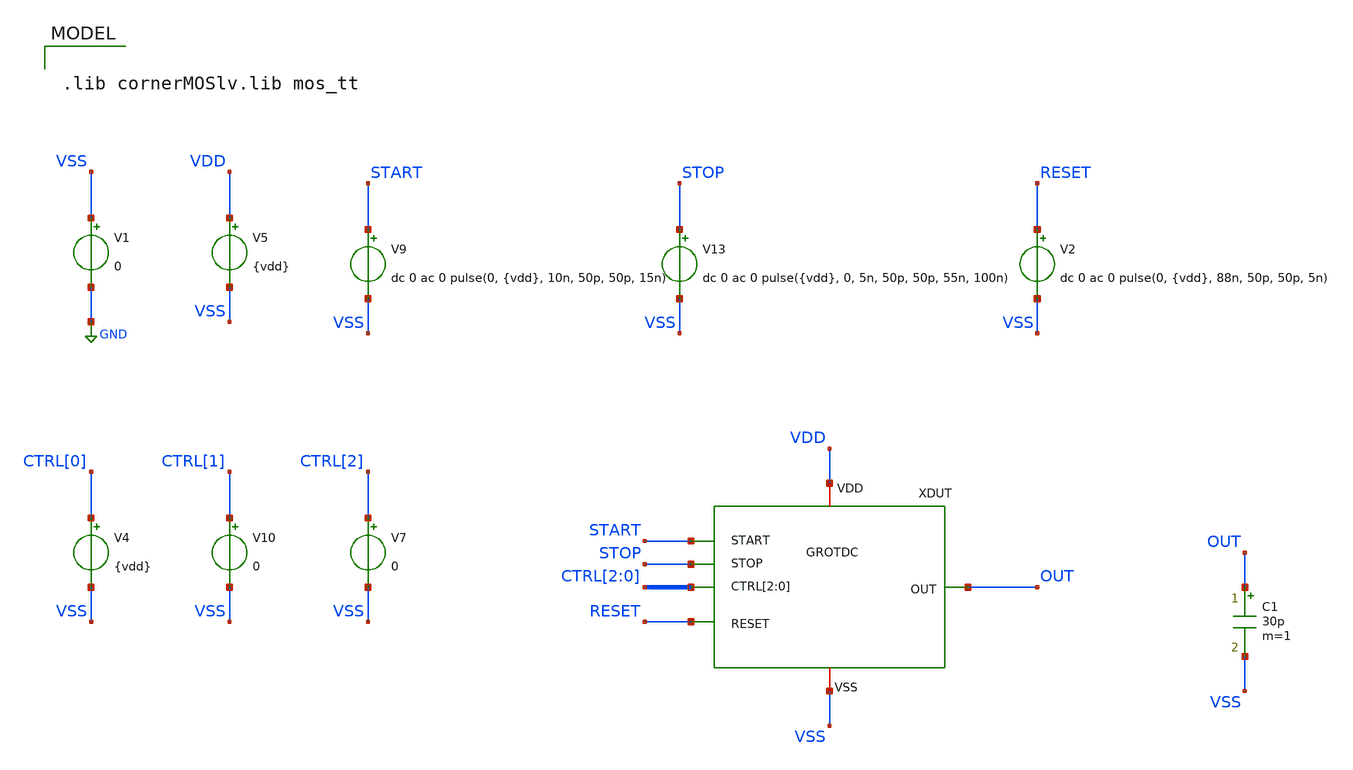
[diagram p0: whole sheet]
** sch_path: ADC8711-main/testbenches/tran/xschem/GROTDC_tb_final.sch
**.subckt GROTDC_tb_final
V1 VSS GND 0
V5 VDD VSS {vdd}
V9 START VSS dc 0 ac 0 pulse(0, {vdd}, 10n, 50p, 50p, 15n)
V13 STOP VSS dc 0 ac 0 pulse({vdd}, 0, 5n, 50p, 50p, 55n, 100n)
XDUT OUT VDD START STOP VSS RESET CTRL[2] CTRL[1] CTRL[0] GROTDC
V4 CTRL[0] VSS {vdd}
V10 CTRL[1] VSS 0
V7 CTRL[2] VSS 0
C1 OUT VSS 30p m=1
V2 RESET VSS dc 0 ac 0 pulse(0, {vdd}, 88n, 50p, 50p, 5n)
**** begin user architecture code

.lib cornerMOSlv.lib mos_tt



.param temp=65
.param vdd=1.2

* Agrega una resistencia gigante en los nodos flotantes
.OPTION RSHUNT=1e9

* Agrega un cap pequeño a cada nodo
* evita dv/dt infinito
.OPTION CSHUNT=1e-15

* Conducción minima en Junturas de diodos
* diodos duros
.options gmin=1e-10

* resistencia serie global (a fuentes ideales e inductores)
.option rseries = 1e-4

* integrador robusto
* ayuda a resolver la no linealidad
.options method=gear

* limita el orden del integrador
* limita cuantos pasos anteriores usa el integrador
.options maxord=2

* tolerancias : error relativo (%) - error absoluto en voltaje - error absoluto en corriente
.options reltol=1e-2 vabstol=1e-4 iabstol=1e-9

* paciencia del solver: DC - Transitorio - Newton interno
.option ITL1=1000 ITL2=400 ITL4=500


* .nodeset all=0

.ic v(START)=0 v(STOP)=0 v(RESET)=0


.ic v(XDUT.IN0)=0 v(XDUT.IN1)=0 v(XDUT.IN2)=0
.ic v(XDUT.K0)=0 v(XDUT.K1)=0 v(XDUT.K2)=0

.ic v(XDUT.D0[0])=0 v(XDUT.D0[1])=0 v(XDUT.D0[2])=0
.ic v(XDUT.D0[3])=0 v(XDUT.D0[4])=0 v(XDUT.D0[5])=0

.ic v(XDUT.D1[0])=0 v(XDUT.D1[1])=0 v(XDUT.D1[2])=0
.ic v(XDUT.D1[3])=0 v(XDUT.D1[4])=0 v(XDUT.D1[5])=0

.ic v(XDUT.D2[0])=0 v(XDUT.D2[1])=0 v(XDUT.D2[2])=0
.ic v(XDUT.D2[3])=0 v(XDUT.D2[4])=0 v(XDUT.D2[5])=0

.ic v(XDUT.C0_B[0])=0 v(XDUT.C1_B[0])=0 v(XDUT.C2_B[0])=0
.ic v(XDUT.C0_B[1])=0 v(XDUT.C1_B[1])=0 v(XDUT.C2_B[1])=0
.ic v(XDUT.C0_B[2])=0 v(XDUT.C1_B[2])=0 v(XDUT.C2_B[2])=0
.ic v(XDUT.C0_B[3])=0 v(XDUT.C1_B[3])=0 v(XDUT.C2_B[3])=0
.ic v(XDUT.C0_B[4])=0 v(XDUT.C1_B[4])=0 v(XDUT.C2_B[4])=0
.ic v(XDUT.C0_B[5])=0 v(XDUT.C1_B[5])=0 v(XDUT.C2_B[5])=0

.ic v(XDUT.S1[0])=0 v(XDUT.S1[1])=0 v(XDUT.S1[2])=0
.ic v(XDUT.S1[3])=0 v(XDUT.S1[4])=0 v(XDUT.S1[5])=0

.ic v(XDUT.COUT1)=0

.ic v(XDUT.S2[0])=0 v(XDUT.S2[1])=0 v(XDUT.S2[2])=0
.ic v(XDUT.S2[3])=0 v(XDUT.S2[4])=0 v(XDUT.S2[5])=0 v(XDUT.S2[6])=0

.ic v(XDUT.COUT2)=0

.ic v(XDUT.ADDER[0])=0 v(XDUT.ADDER[1])=0 v(XDUT.ADDER[2])=0
.ic v(XDUT.ADDER[3])=0 v(XDUT.ADDER[4])=0 v(XDUT.ADDER[5])=0
.ic v(XDUT.ADDER[6])=0 v(XDUT.ADDER[7])=0


.control

* Sources
save v(START) v(STOP) v(RESET)

save v(XDUT.START_PAD) v(XDUT.STOP_PAD) v(XDUT.RESET_PAD)
save v(XDUT.VSS) v(XDUT.VDD) v(XDUT.EN)


* GRO
save v(XDUT.IN0) v(XDUT.IN1) v(XDUT.IN2)


* Buffers
save v(XDUT.K0) v(XDUT.K1) v(XDUT.K2)

* Delay cell
save v(XDUT.DRV_STOP) v(XDUT.DECLK) v(XDUT.DECLK2)

* Counters Reg
* C0_B
save v(XDUT.net1_0)
save v(XDUT.net1_1)
save v(XDUT.net1_2)
save v(XDUT.net1_3)
save v(XDUT.net1_4)
save v(XDUT.net1_5)

* C1_B
save v(XDUT.net2_0)
save v(XDUT.net2_1)
save v(XDUT.net2_2)
save v(XDUT.net2_3)
save v(XDUT.net2_4)
save v(XDUT.net2_5)

* C2_B
save v(XDUT.net3_0)
save v(XDUT.net3_1)
save v(XDUT.net3_2)
save v(XDUT.net3_3)
save v(XDUT.net3_4)
save v(XDUT.net3_5)

* Counters regs
save v(XDUT.D0[0]) v(XDUT.D0[1]) v(XDUT.D0[2])
save v(XDUT.D0[3]) v(XDUT.D0[4]) v(XDUT.D0[5])

save v(XDUT.D1[0]) v(XDUT.D1[1]) v(XDUT.D1[2])
save v(XDUT.D1[3]) v(XDUT.D1[4]) v(XDUT.D1[5])

save v(XDUT.D2[0]) v(XDUT.D2[1]) v(XDUT.D2[2])
save v(XDUT.D2[3]) v(XDUT.D2[4]) v(XDUT.D2[5])

* FA
save v(XDUT.S1[0]) v(XDUT.S1[1]) v(XDUT.S1[2])
save v(XDUT.S1[3]) v(XDUT.S1[4]) v(XDUT.S1[5])

save v(XDUT.COUT1)

save v(XDUT.S2[0]) v(XDUT.S2[1]) v(XDUT.S2[2])
save v(XDUT.S2[3]) v(XDUT.S2[4]) v(XDUT.S2[5]) v(XDUT.S2[6])

save v(XDUT.COUT2)


* FA Regs
save v(XDUT.ADDER[0]) v(XDUT.ADDER[1]) v(XDUT.ADDER[2])
save v(XDUT.ADDER[3]) v(XDUT.ADDER[4]) v(XDUT.ADDER[5])
save v(XDUT.ADDER[6]) v(XDUT.ADDER[7])

save v(OUT)

* uic: saltearse el punto de operación
*tran 5p 100n 0 5p uic

* .tran <tstep> <tstop> [tstart] [tmax] [uic]
* tmax Limita el paso máximo que puede usar el integrador
tran 5p 90n 0 10p


write GRO_TDC_tb_final.raw

.endc


**** end user architecture code
**.ends
.GLOBAL GND
.end
